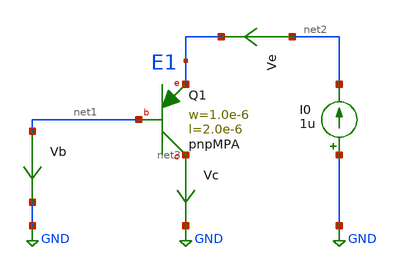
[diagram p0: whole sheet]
** sch_path: ihp-sg13g2/xschem_libs/sg13g2_tests_ase/dc_pnpMPA/schematic/dc_pnpMPA.sch
* Copyright 2023 IHP PDK Authors
**.subckt dc_pnpMPA
Ve net2 E1 0
.save i(ve)
Vb net1 GND 0
.save i(vb)
Vc net3 GND 0
.save i(vc)
I0 GND net2 1u
XQ1 net3 net1 E1 pnpMPA a=2p p=6u m=1
**.ends
.GLOBAL GND
.end
